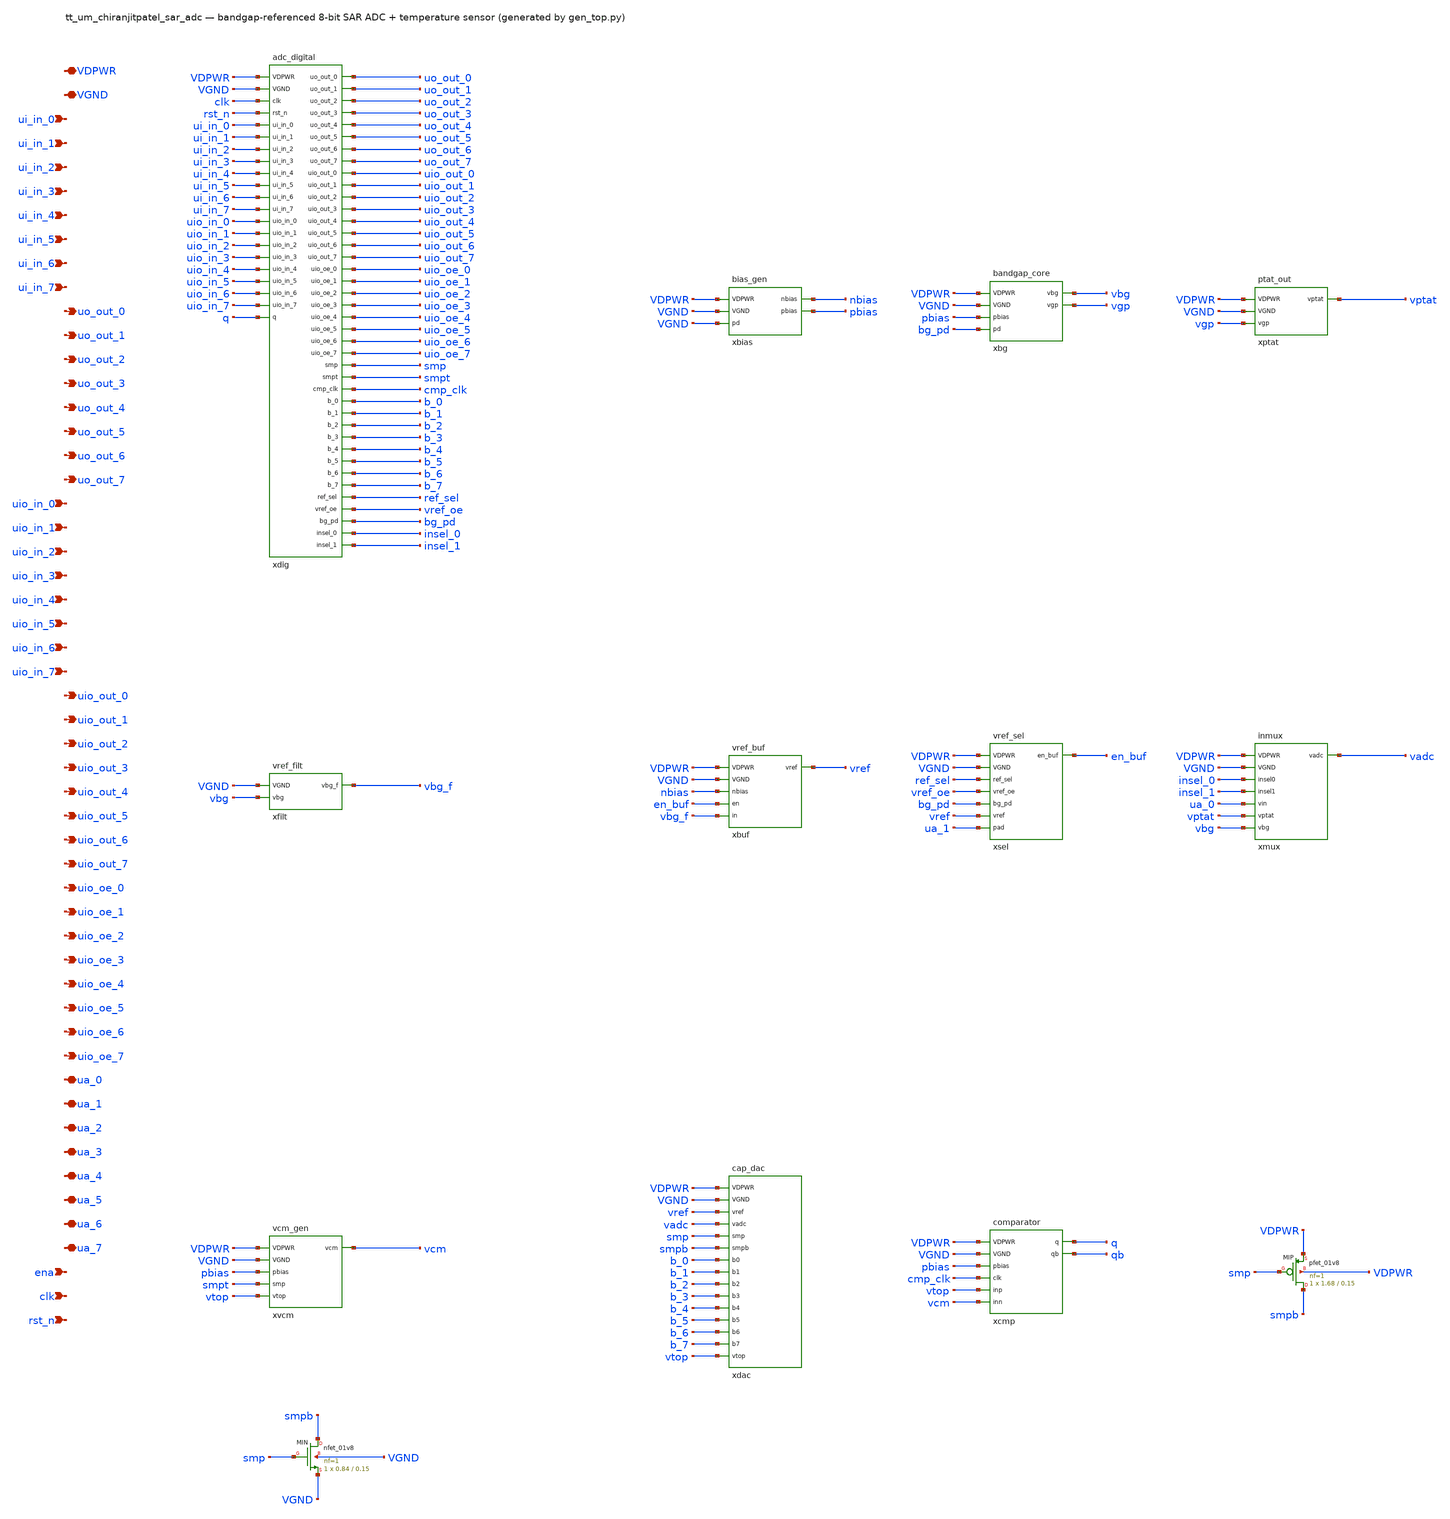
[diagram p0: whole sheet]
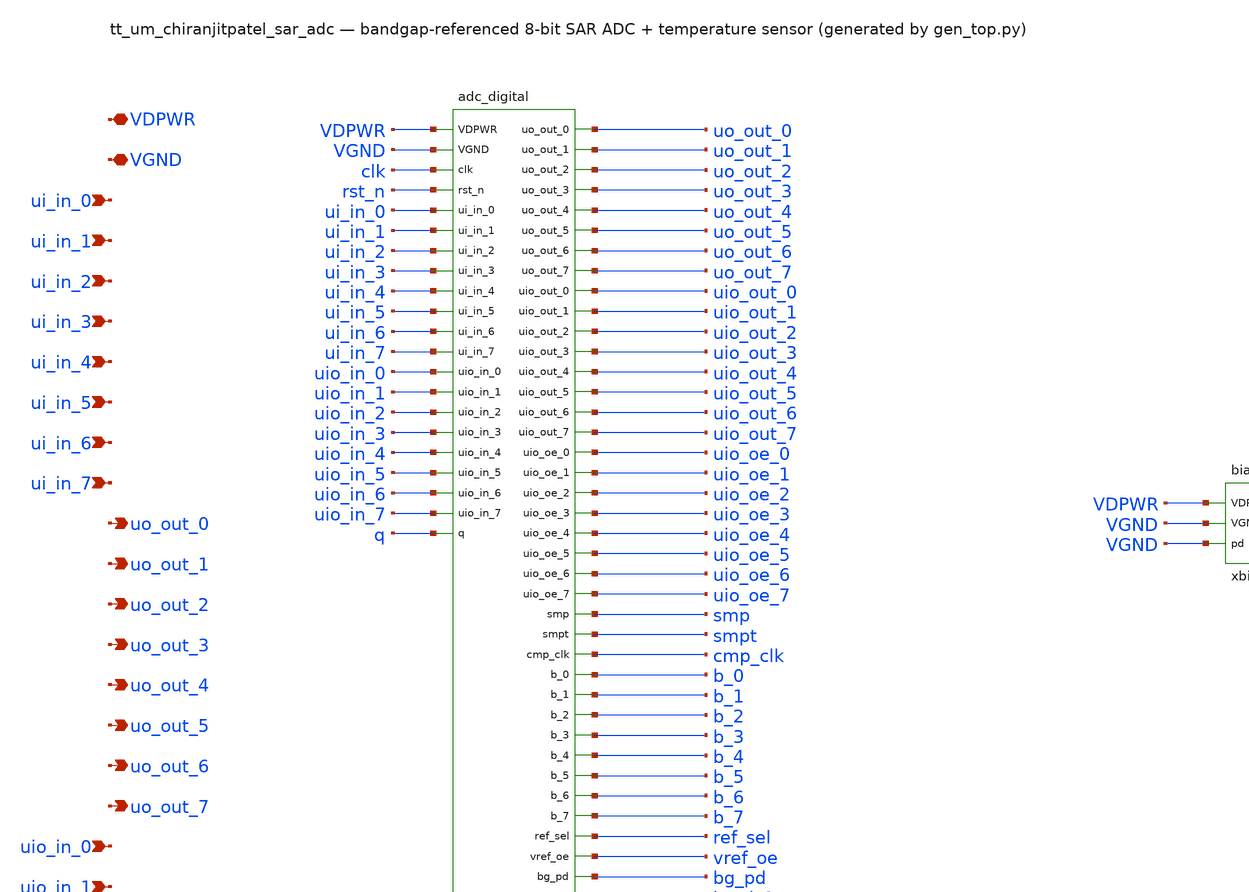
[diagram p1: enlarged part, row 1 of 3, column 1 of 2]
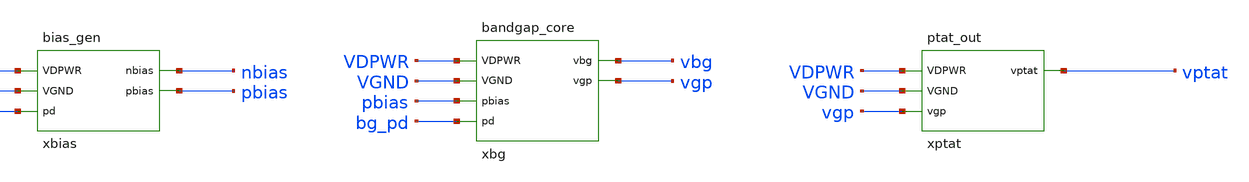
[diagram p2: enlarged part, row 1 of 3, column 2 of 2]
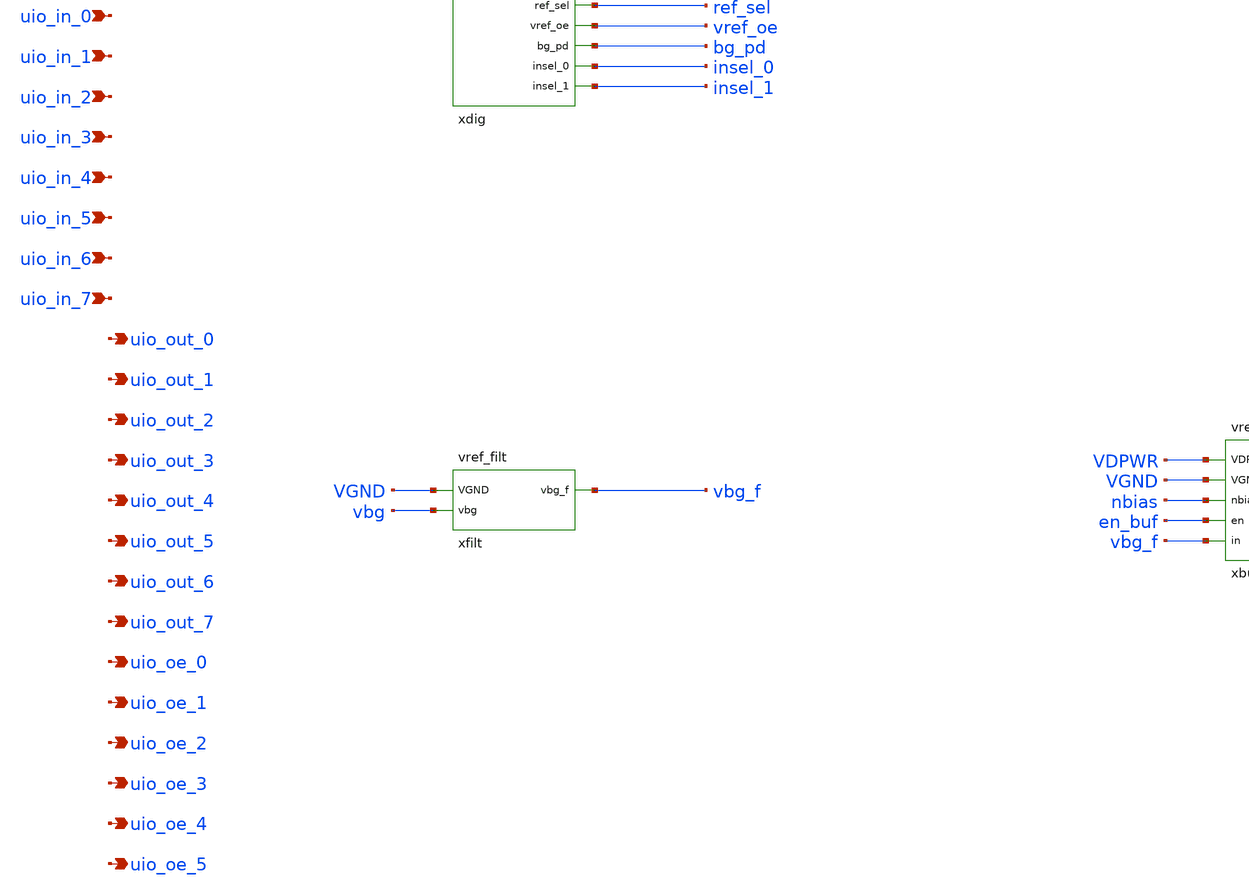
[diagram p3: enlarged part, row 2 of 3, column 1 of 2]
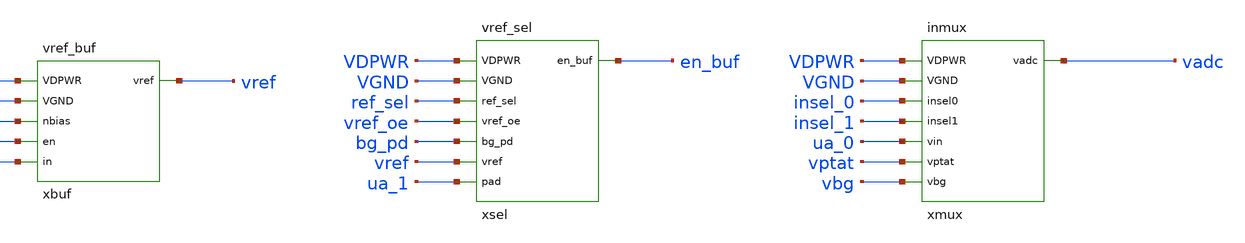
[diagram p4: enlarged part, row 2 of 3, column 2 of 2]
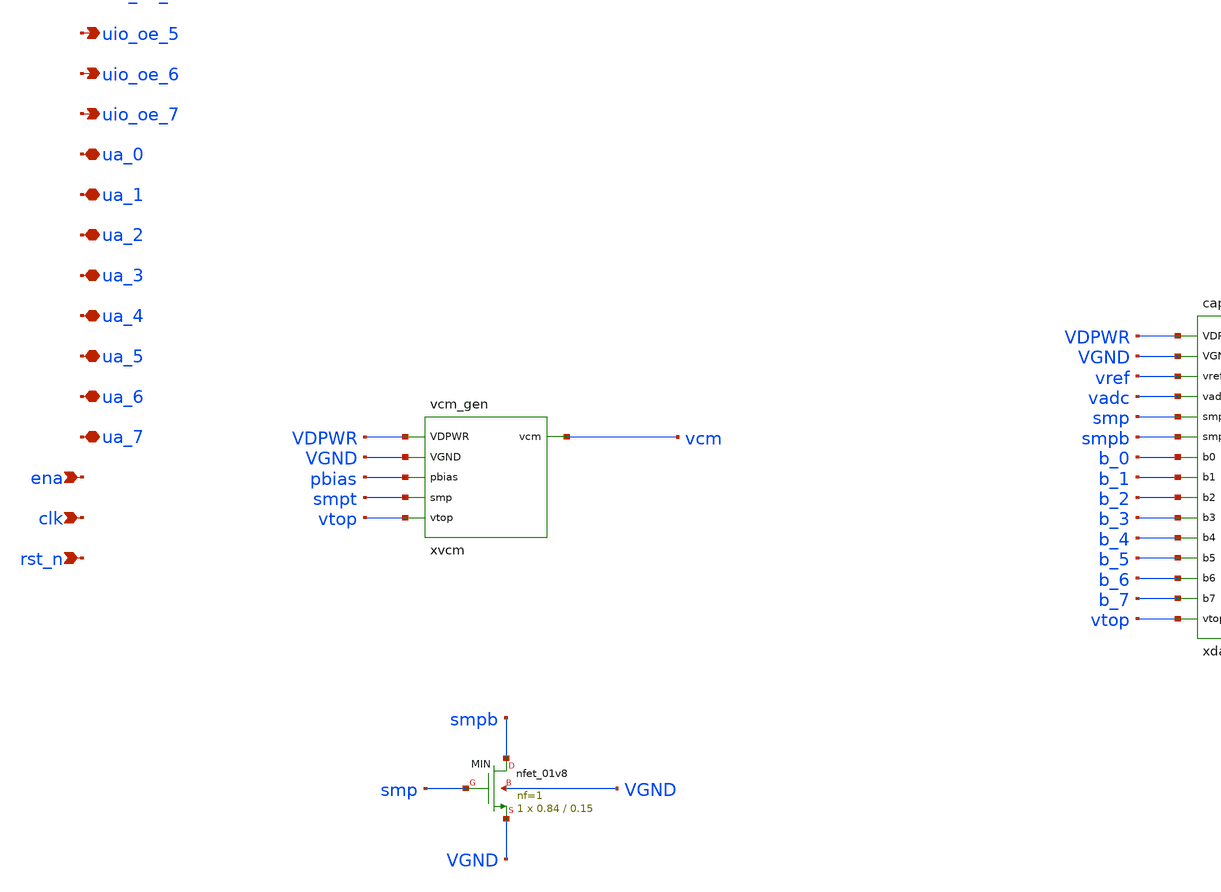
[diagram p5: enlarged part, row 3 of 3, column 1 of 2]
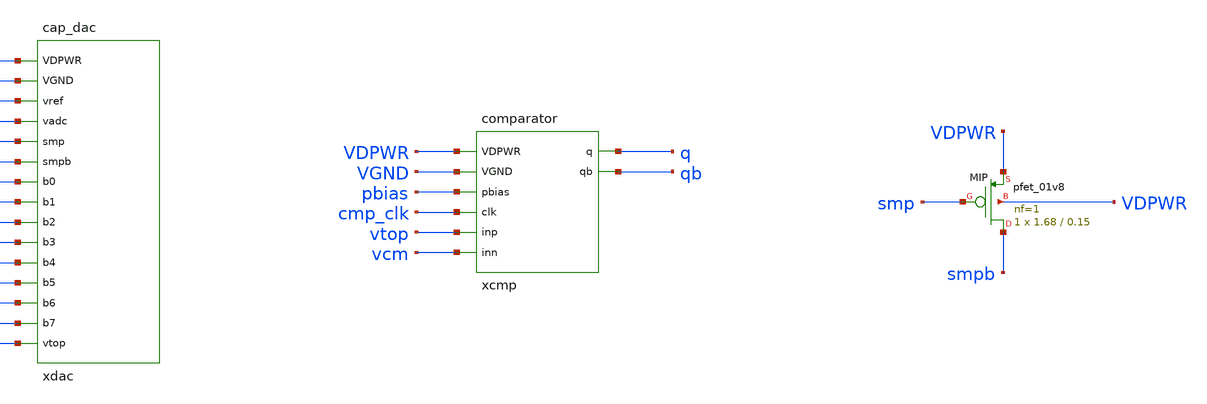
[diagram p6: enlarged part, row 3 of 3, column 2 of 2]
** sch_path: xschem/tt_um_chiranjitpatel_sar_adc.sch
**.subckt tt_um_chiranjitpatel_sar_adc VDPWR VGND ui_in_0 ui_in_1 ui_in_2 ui_in_3 ui_in_4 ui_in_5
*+ ui_in_6 ui_in_7 uo_out_0 uo_out_1 uo_out_2 uo_out_3 uo_out_4 uo_out_5 uo_out_6 uo_out_7 uio_in_0 uio_in_1
*+ uio_in_2 uio_in_3 uio_in_4 uio_in_5 uio_in_6 uio_in_7 uio_out_0 uio_out_1 uio_out_2 uio_out_3 uio_out_4
*+ uio_out_5 uio_out_6 uio_out_7 uio_oe_0 uio_oe_1 uio_oe_2 uio_oe_3 uio_oe_4 uio_oe_5 uio_oe_6 uio_oe_7 ua_0
*+ ua_1 ua_2 ua_3 ua_4 ua_5 ua_6 ua_7 ena clk rst_n
*.iopin VDPWR
*.iopin VGND
*.ipin ui_in_0
*.ipin ui_in_1
*.ipin ui_in_2
*.ipin ui_in_3
*.ipin ui_in_4
*.ipin ui_in_5
*.ipin ui_in_6
*.ipin ui_in_7
*.opin uo_out_0
*.opin uo_out_1
*.opin uo_out_2
*.opin uo_out_3
*.opin uo_out_4
*.opin uo_out_5
*.opin uo_out_6
*.opin uo_out_7
*.ipin uio_in_0
*.ipin uio_in_1
*.ipin uio_in_2
*.ipin uio_in_3
*.ipin uio_in_4
*.ipin uio_in_5
*.ipin uio_in_6
*.ipin uio_in_7
*.opin uio_out_0
*.opin uio_out_1
*.opin uio_out_2
*.opin uio_out_3
*.opin uio_out_4
*.opin uio_out_5
*.opin uio_out_6
*.opin uio_out_7
*.opin uio_oe_0
*.opin uio_oe_1
*.opin uio_oe_2
*.opin uio_oe_3
*.opin uio_oe_4
*.opin uio_oe_5
*.opin uio_oe_6
*.opin uio_oe_7
*.iopin ua_0
*.iopin ua_1
*.iopin ua_2
*.iopin ua_3
*.iopin ua_4
*.iopin ua_5
*.iopin ua_6
*.iopin ua_7
*.ipin ena
*.ipin clk
*.ipin rst_n
xdig VDPWR VGND clk rst_n ui_in_0 ui_in_1 ui_in_2 ui_in_3 ui_in_4 ui_in_5 ui_in_6 ui_in_7 uio_in_0
+ uio_in_1 uio_in_2 uio_in_3 uio_in_4 uio_in_5 uio_in_6 uio_in_7 q uo_out_0 uo_out_1 uo_out_2 uo_out_3
+ uo_out_4 uo_out_5 uo_out_6 uo_out_7 uio_out_0 uio_out_1 uio_out_2 uio_out_3 uio_out_4 uio_out_5 uio_out_6
+ uio_out_7 uio_oe_0 uio_oe_1 uio_oe_2 uio_oe_3 uio_oe_4 uio_oe_5 uio_oe_6 uio_oe_7 smp smpt cmp_clk b_0 b_1
+ b_2 b_3 b_4 b_5 b_6 b_7 ref_sel vref_oe bg_pd insel_0 insel_1 adc_digital
xbias VDPWR VGND VGND nbias pbias bias_gen
xbg VDPWR VGND pbias bg_pd vbg vgp bandgap_core
xptat VDPWR VGND vgp vptat ptat_out
xfilt VGND vbg vbg_f vref_filt
xbuf VDPWR VGND nbias en_buf vbg_f vref vref_buf
xsel VDPWR VGND ref_sel vref_oe bg_pd vref ua_1 en_buf vref_sel
xmux VDPWR VGND insel_0 insel_1 ua_0 vptat vbg vadc inmux
xvcm VDPWR VGND pbias smpt vtop vcm vcm_gen
xdac VDPWR VGND vref vadc smp smpb b_0 b_1 b_2 b_3 b_4 b_5 b_6 b_7 vtop cap_dac
xcmp VDPWR VGND pbias cmp_clk vtop vcm q qb comparator
XMIP smpb smp VDPWR VDPWR sky130_fd_pr__pfet_01v8 L=0.15 W=1.68 nf=1 ad='int((nf+1)/2) * W/nf * 0.29'
+ as='int((nf+2)/2) * W/nf * 0.29' pd='2*int((nf+1)/2) * (W/nf + 0.29)' ps='2*int((nf+2)/2) * (W/nf + 0.29)'
+ nrd='0.29 / W' nrs='0.29 / W' sa=0 sb=0 sd=0 mult=1 m=1
XMIN smpb smp VGND VGND sky130_fd_pr__nfet_01v8 L=0.15 W=0.84 nf=1 ad='int((1 + 1)/2) * 0.84 / 1 * 0.29'
+ as='int((1 + 2)/2) * 0.84 / 1 * 0.29' pd='2*int((1 + 1)/2) * (0.84 / 1 + 0.29)' ps='2*int((1 + 2)/2) * (0.84 / 1 + 0.29)'
+ nrd='0.29 / 0.84 ' nrs='0.29 / 0.84 ' sa=0 sb=0 sd=0 mult=1 m=1
**.ends
.end
